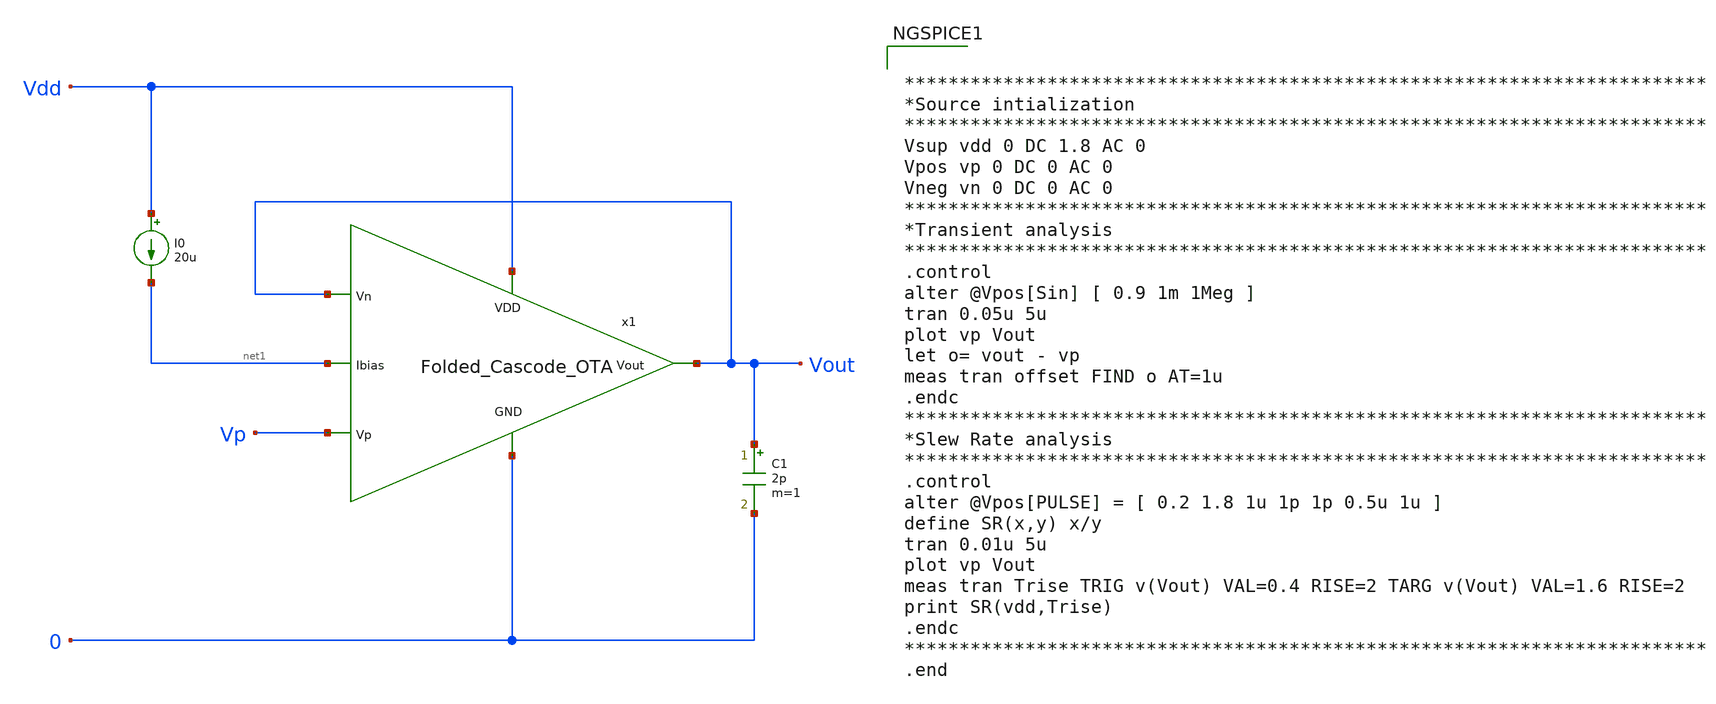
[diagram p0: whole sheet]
** sch_path: Analog_Blocks/OTA/Testbench/Folded_Cascode/Transistor1.8v/Folded_Cascode1.8v_meas_Transient.sch
**.subckt Folded_Cascode1.8v_meas_Transient
I0 Vdd net1 20u
C1 Vout 0 2p m=1
x1 Vdd Vout Vp Vout net1 0 Folded_Cascode_OTA
**** begin user architecture code

.include ~/Analog_blocks/models/skywater-pdk/libraries/sky130_fd_pr/latest/cells/nfet_01v8/sky130_fd_pr__nfet_01v8__tt.corner.spice
.include ~/Analog_blocks/models/skywater-pdk/libraries/sky130_fd_pr/latest/cells/nfet_01v8_lvt/sky130_fd_pr__nfet_01v8_lvt__tt.corner.spice
.include ~/Analog_blocks/models/skywater-pdk/libraries/sky130_fd_pr/latest/cells/pfet_01v8/sky130_fd_pr__pfet_01v8__tt.corner.spice
.include ~/Analog_blocks/models/skywater-pdk/libraries/sky130_fd_pr/latest/cells/nfet_03v3_nvt/sky130_fd_pr__nfet_03v3_nvt__tt.corner.spice
.include ~/Analog_blocks/models/skywater-pdk/libraries/sky130_fd_pr/latest/cells/nfet_05v0_nvt/sky130_fd_pr__nfet_05v0_nvt__tt.corner.spice
.include ~/Analog_blocks/models/skywater-pdk/libraries/sky130_fd_pr/latest/cells/esd_nfet_01v8/sky130_fd_pr__esd_nfet_01v8__tt.corner.spice
.include ~/Analog_blocks/models/skywater-pdk/libraries/sky130_fd_pr/latest/cells/pfet_01v8_lvt/sky130_fd_pr__pfet_01v8_lvt__tt.corner.spice
.include ~/Analog_blocks/models/skywater-pdk/libraries/sky130_fd_pr/latest/cells/pfet_01v8_hvt/sky130_fd_pr__pfet_01v8_hvt__tt.corner.spice
.include ~/Analog_blocks/models/skywater-pdk/libraries/sky130_fd_pr/latest/cells/esd_pfet_g5v0d10v5/sky130_fd_pr__esd_pfet_g5v0d10v5__tt.corner.spice
.include ~/Analog_blocks/models/skywater-pdk/libraries/sky130_fd_pr/latest/cells/pfet_g5v0d10v5/sky130_fd_pr__pfet_g5v0d10v5__tt.corner.spice
.include ~/Analog_blocks/models/skywater-pdk/libraries/sky130_fd_pr/latest/cells/pfet_g5v0d16v0/sky130_fd_pr__pfet_g5v0d16v0__tt.corner.spice
.include ~/Analog_blocks/models/skywater-pdk/libraries/sky130_fd_pr/latest/cells/nfet_g5v0d10v5/sky130_fd_pr__nfet_g5v0d10v5__tt.corner.spice
.include ~/Analog_blocks/models/skywater-pdk/libraries/sky130_fd_pr/latest/cells/nfet_g5v0d16v0/sky130_fd_pr__nfet_g5v0d16v0__tt_discrete.corner.spice
.include ~/Analog_blocks/models/skywater-pdk/libraries/sky130_fd_pr/latest/cells/esd_nfet_g5v0d10v5/sky130_fd_pr__esd_nfet_g5v0d10v5__tt.corner.spice
.include ~/Analog_blocks/models/skywater-pdk/libraries/sky130_fd_pr/latest/models/corners/tt/nonfet.spice
* Mismatch parameters
.include ~/Analog_blocks/models/skywater-pdk/libraries/sky130_fd_pr/latest/cells/nfet_01v8/sky130_fd_pr__nfet_01v8__mismatch.corner.spice
.include ~/Analog_blocks/models/skywater-pdk/libraries/sky130_fd_pr/latest/cells/pfet_01v8/sky130_fd_pr__pfet_01v8__mismatch.corner.spice
.include ~/Analog_blocks/models/skywater-pdk/libraries/sky130_fd_pr/latest/cells/nfet_01v8_lvt/sky130_fd_pr__nfet_01v8_lvt__mismatch.corner.spice
.include ~/Analog_blocks/models/skywater-pdk/libraries/sky130_fd_pr/latest/cells/pfet_01v8_lvt/sky130_fd_pr__pfet_01v8_lvt__mismatch.corner.spice
.include ~/Analog_blocks/models/skywater-pdk/libraries/sky130_fd_pr/latest/cells/pfet_01v8_hvt/sky130_fd_pr__pfet_01v8_hvt__mismatch.corner.spice
.include ~/Analog_blocks/models/skywater-pdk/libraries/sky130_fd_pr/latest/cells/nfet_g5v0d10v5/sky130_fd_pr__nfet_g5v0d10v5__mismatch.corner.spice
.include ~/Analog_blocks/models/skywater-pdk/libraries/sky130_fd_pr/latest/cells/pfet_g5v0d10v5/sky130_fd_pr__pfet_g5v0d10v5__mismatch.corner.spice
.include ~/Analog_blocks/models/skywater-pdk/libraries/sky130_fd_pr/latest/cells/nfet_05v0_nvt/sky130_fd_pr__nfet_05v0_nvt__mismatch.corner.spice
.include ~/Analog_blocks/models/skywater-pdk/libraries/sky130_fd_pr/latest/cells/nfet_03v3_nvt/sky130_fd_pr__nfet_03v3_nvt__mismatch.corner.spice
* Resistor
.include ~/Analog_blocks/models/skywater-pdk/libraries/sky130_fd_pr/latest/models/r+c/res_typical__cap_typical.spice
.include ~/Analog_blocks/models/skywater-pdk/libraries/sky130_fd_pr/latest/models/r+c/res_typical__cap_typical__lin.spice
* Special cells
.include ~/Analog_blocks/models/skywater-pdk/libraries/sky130_fd_pr/latest/models/corners/tt/specialized_cells.spice
* All models
.include ~/Analog_blocks/models/skywater-pdk/libraries/sky130_fd_pr/latest/models/all.spice
* Corner
.include ~/Analog_blocks/models/skywater-pdk/libraries/sky130_fd_pr/latest/models/corners/tt/rf.spice



*************************************************************************
*Source intialization
*************************************************************************
Vsup vdd 0 DC 1.8 AC 0
Vpos vp 0 DC 0 AC 0
Vneg vn 0 DC 0 AC 0
*************************************************************************
*Transient analysis
*************************************************************************
.control
alter @Vpos[Sin] [ 0.9 1m 1Meg ]
tran 0.05u 5u
plot vp Vout
let o= vout - vp
meas tran offset FIND o AT=1u
.endc
*************************************************************************
*Slew Rate analysis
*************************************************************************
.control
alter @Vpos[PULSE] = [ 0.2 1.8 1u 1p 1p 0.5u 1u ]
define SR(x,y) x/y
tran 0.01u 5u
plot vp Vout
meas tran Trise TRIG v(Vout) VAL=0.4 RISE=2 TARG v(Vout) VAL=1.6 RISE=2
print SR(vdd,Trise)
.endc
*************************************************************************
.end


**** end user architecture code
**.ends
.end
